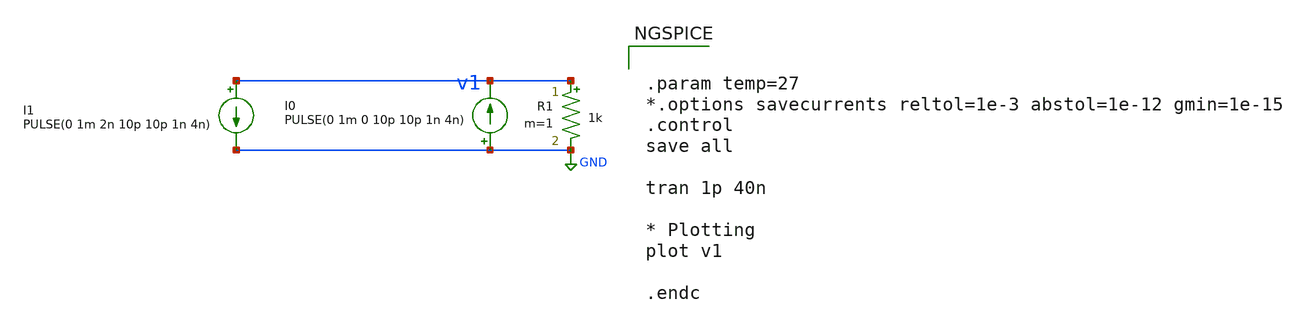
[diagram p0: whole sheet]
** sch_path: xschem/untitled-1.sch
**.subckt untitled-1
I0 GND v1 PULSE(0 1m 0 10p 10p 1n 4n)
R1 v1 GND 1k m=1
I1 v1 GND PULSE(0 1m 2n 10p 10p 1n 4n)
**** begin user architecture code


.param temp=27
*.options savecurrents reltol=1e-3 abstol=1e-12 gmin=1e-15
.control
save all

tran 1p 40n

* Plotting
plot v1

.endc

**** end user architecture code
**.ends
.GLOBAL GND
.end
